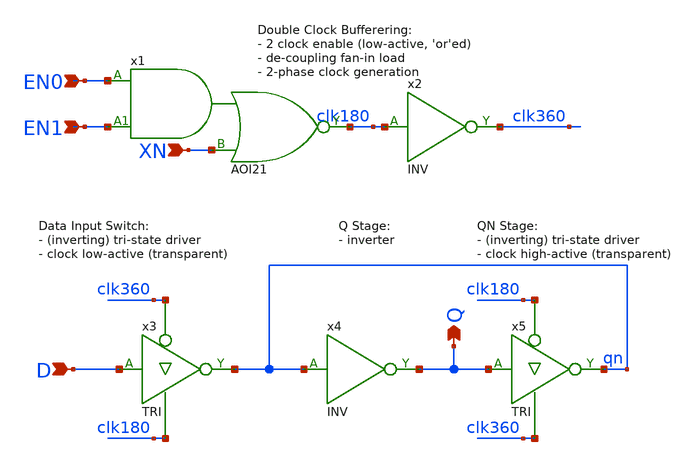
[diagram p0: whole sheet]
** sch_path: Sources/crafted/LATNEE.sch
**.subckt LATNEE XN D Q EN0 EN1
*.ipin XN
*.ipin D
*.opin Q
*.ipin EN0
*.ipin EN1
x1 EN0 EN1 XN clk180 VDD GND AOI21 Wmin=1.5u Lmin=1u g=2 m=1
x2 clk180 clk360 VDD GND INV Wmin=1.5u Lmin=1u g=2 m=1
x3 D clk360 clk180 qn VDD GND TRI Wmin=1.5u Lmin=1u g=2 m=1
x5 Q clk180 clk360 qn VDD GND TRI Wmin=1.5u Lmin=1u g=2 m=1
x4 qn Q VDD GND INV Wmin=1.5u Lmin=1u g=2 m=1
**.ends
.end
